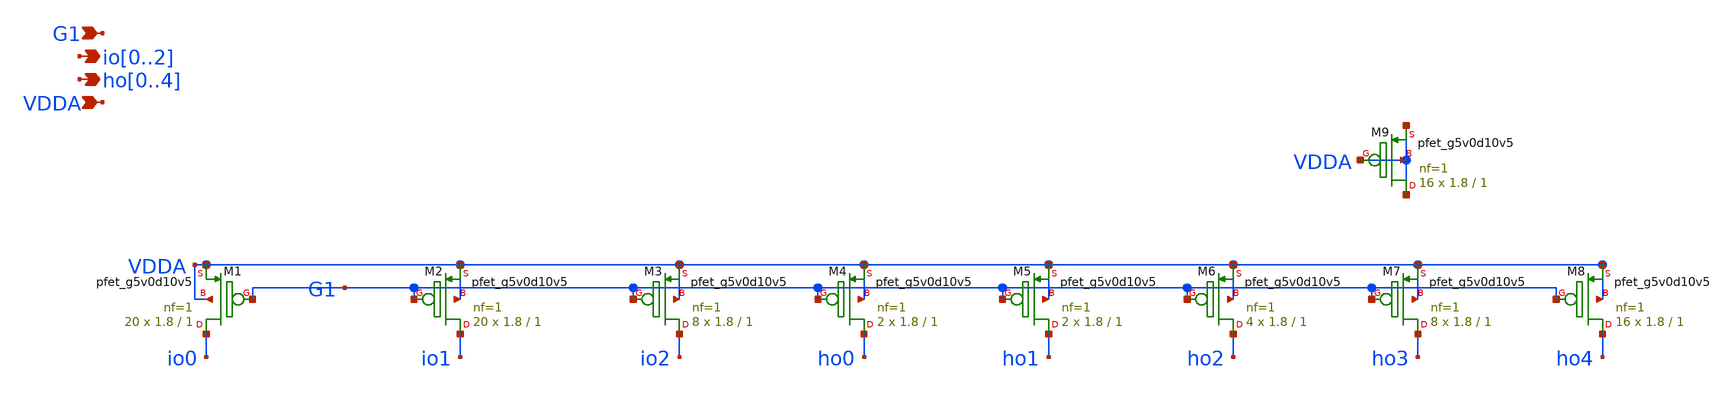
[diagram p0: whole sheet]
** sch_path: xschem/cm_pcell1.sch
**.subckt cm_pcell1 G1 io0,io1,io2 VDDA ho0,ho1,ho2,ho3,ho4
*.ipin G1
*.opin io0,io1,io2
*.ipin VDDA
*.opin ho0,ho1,ho2,ho3,ho4
XM1 io0 G1 VDDA VDDA sky130_fd_pr__pfet_g5v0d10v5 L=1 W=1.8 nf=1 ad='int((nf+1)/2) * W/nf * 0.29' as='int((nf+2)/2) * W/nf * 0.29'
+ pd='2*int((nf+1)/2) * (W/nf + 0.29)' ps='2*int((nf+2)/2) * (W/nf + 0.29)' nrd='0.29 / W' nrs='0.29 / W'
+ sa=0 sb=0 sd=0 mult=20 m=20
XM2 io1 G1 VDDA VDDA sky130_fd_pr__pfet_g5v0d10v5 L=1 W=1.8 nf=1 ad='int((nf+1)/2) * W/nf * 0.29' as='int((nf+2)/2) * W/nf * 0.29'
+ pd='2*int((nf+1)/2) * (W/nf + 0.29)' ps='2*int((nf+2)/2) * (W/nf + 0.29)' nrd='0.29 / W' nrs='0.29 / W'
+ sa=0 sb=0 sd=0 mult=20 m=20
XM3 io2 G1 VDDA VDDA sky130_fd_pr__pfet_g5v0d10v5 L=1 W=1.8 nf=1 ad='int((nf+1)/2) * W/nf * 0.29' as='int((nf+2)/2) * W/nf * 0.29'
+ pd='2*int((nf+1)/2) * (W/nf + 0.29)' ps='2*int((nf+2)/2) * (W/nf + 0.29)' nrd='0.29 / W' nrs='0.29 / W'
+ sa=0 sb=0 sd=0 mult=8 m=8
XM4 ho0 G1 VDDA VDDA sky130_fd_pr__pfet_g5v0d10v5 L=1 W=1.8 nf=1 ad='int((nf+1)/2) * W/nf * 0.29' as='int((nf+2)/2) * W/nf * 0.29'
+ pd='2*int((nf+1)/2) * (W/nf + 0.29)' ps='2*int((nf+2)/2) * (W/nf + 0.29)' nrd='0.29 / W' nrs='0.29 / W'
+ sa=0 sb=0 sd=0 mult=2 m=2
XM6 ho2 G1 VDDA VDDA sky130_fd_pr__pfet_g5v0d10v5 L=1 W=1.8 nf=1 ad='int((nf+1)/2) * W/nf * 0.29' as='int((nf+2)/2) * W/nf * 0.29'
+ pd='2*int((nf+1)/2) * (W/nf + 0.29)' ps='2*int((nf+2)/2) * (W/nf + 0.29)' nrd='0.29 / W' nrs='0.29 / W'
+ sa=0 sb=0 sd=0 mult=4 m=4
XM7 ho3 G1 VDDA VDDA sky130_fd_pr__pfet_g5v0d10v5 L=1 W=1.8 nf=1 ad='int((nf+1)/2) * W/nf * 0.29' as='int((nf+2)/2) * W/nf * 0.29'
+ pd='2*int((nf+1)/2) * (W/nf + 0.29)' ps='2*int((nf+2)/2) * (W/nf + 0.29)' nrd='0.29 / W' nrs='0.29 / W'
+ sa=0 sb=0 sd=0 mult=8 m=8
XM8 ho4 G1 VDDA VDDA sky130_fd_pr__pfet_g5v0d10v5 L=1 W=1.8 nf=1 ad='int((nf+1)/2) * W/nf * 0.29' as='int((nf+2)/2) * W/nf * 0.29'
+ pd='2*int((nf+1)/2) * (W/nf + 0.29)' ps='2*int((nf+2)/2) * (W/nf + 0.29)' nrd='0.29 / W' nrs='0.29 / W'
+ sa=0 sb=0 sd=0 mult=16 m=16
XM5 ho1 G1 VDDA VDDA sky130_fd_pr__pfet_g5v0d10v5 L=1 W=1.8 nf=1 ad='int((nf+1)/2) * W/nf * 0.29' as='int((nf+2)/2) * W/nf * 0.29'
+ pd='2*int((nf+1)/2) * (W/nf + 0.29)' ps='2*int((nf+2)/2) * (W/nf + 0.29)' nrd='0.29 / W' nrs='0.29 / W'
+ sa=0 sb=0 sd=0 mult=2 m=2
XM9 VDDA VDDA VDDA VDDA sky130_fd_pr__pfet_g5v0d10v5 L=1 W=1.8 nf=1 ad='int((nf+1)/2) * W/nf * 0.29'
+ as='int((nf+2)/2) * W/nf * 0.29' pd='2*int((nf+1)/2) * (W/nf + 0.29)' ps='2*int((nf+2)/2) * (W/nf + 0.29)'
+ nrd='0.29 / W' nrs='0.29 / W' sa=0 sb=0 sd=0 mult=16 m=16
**.ends
.end
